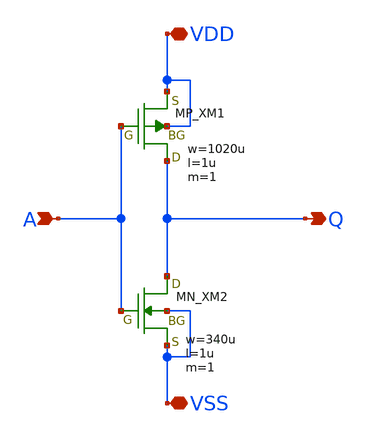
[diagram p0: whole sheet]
** sch_path: schematic/20250924_OSS_Workshop/ishikai/inverter/inv_big100.sch
**.subckt inv_big100 A VDD VSS Q
*.ipin A
*.iopin VDD
*.iopin VSS
*.opin Q
XM1 Q A VDD VDD PMOS w=1020u l=1u as=0 ad=0 ps=0 pd=0 nrd=0 nrs=0 m=1
XM2 Q A VSS VSS NMOS w=340u l=1u as=0 ad=0 ps=0 pd=0 nrd=0 nrs=0 m=1
**.ends
.end
